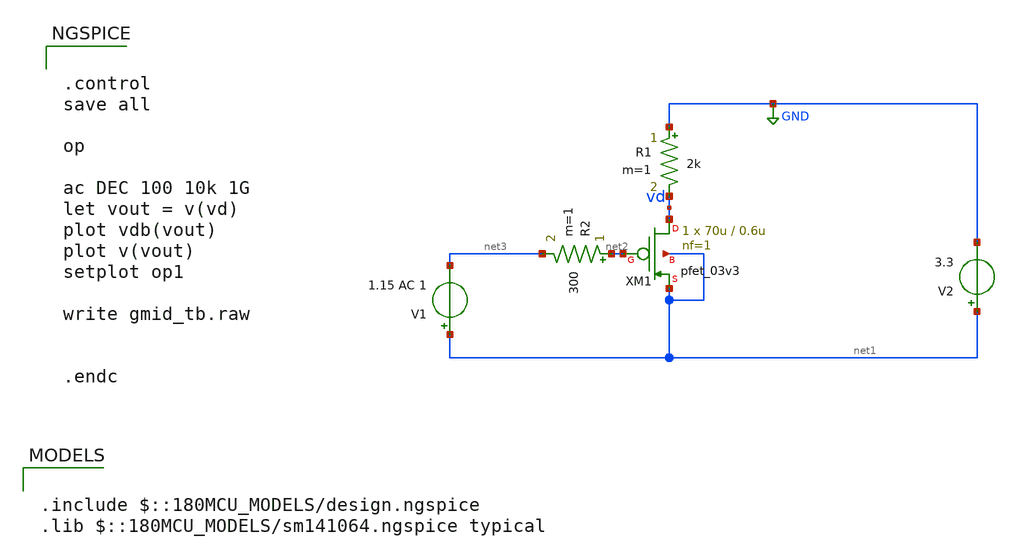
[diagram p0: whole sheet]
** sch_path: designs/switch_matrix_gf180mcu_9t5v0-main/designs/libs/tb_analog/tb_ota_5t_dc/gmid_pfet_tb.sch
**.subckt gmid_pfet_tb
V1 net1 net3 1.15 AC 1
V2 net1 GND 3.3
R1 GND vd 2k m=1
R2 net2 net3 300 m=1
XM1 vd net2 net1 net1 pfet_03v3 L=0.6u W=70u nf=1 ad='int((nf+1)/2) * W/nf * 0.18u' as='int((nf+2)/2) * W/nf * 0.18u'
+ pd='2*int((nf+1)/2) * (W/nf + 0.18u)' ps='2*int((nf+2)/2) * (W/nf + 0.18u)' nrd='0.18u / W' nrs='0.18u / W'
+ sa=0 sb=0 sd=0 m=1
**** begin user architecture code

.include $::180MCU_MODELS/design.ngspice
.lib $::180MCU_MODELS/sm141064.ngspice typical



.control
save all

op

ac DEC 100 10k 1G
let vout = v(vd)
plot vdb(vout)
plot v(vout)
setplot op1

write gmid_tb.raw


.endc


**** end user architecture code
**.ends
.GLOBAL GND
.end
